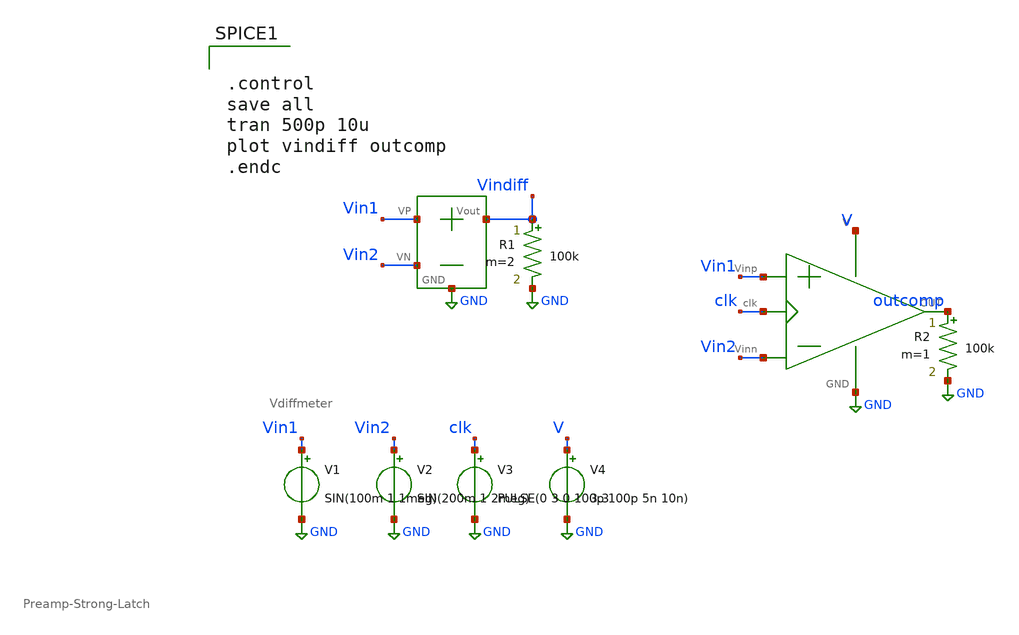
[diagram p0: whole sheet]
** sch_path: SAR_ADC/xschem/test/comp_full_tb/100mv_sin_1meg-200mv_sin_2meg__tb.sch
**.subckt 100mv_sin_1meg-200mv_sin_2meg__tb
X1 V GND Vin1 Vin2 outcomp clk Preamp-Strong-Latch
V1 Vin1 GND SIN(100m 1 1meg)
V2 Vin2 GND SIN(200m 1 2meg)
V3 clk GND PULSE(0 3 0 100p 100p 5n 10n)
V4 V GND 3.3
X2 Vin1 Vin2 Vindiff GND Vdiffmeter
R1 Vindiff GND 100k m=2
R2 outcomp GND 100k m=1
**** begin user architecture code


.control
save all
tran 500p 10u
plot vindiff outcomp
.endc


.include /foss/pdks/gf180mcuC/libs.tech/ngspice/design.ngspice
.lib /foss/pdks/gf180mcuC/libs.tech/ngspice/sm141064.ngspice typical

**** end user architecture code
**.ends
.GLOBAL GND
.end
